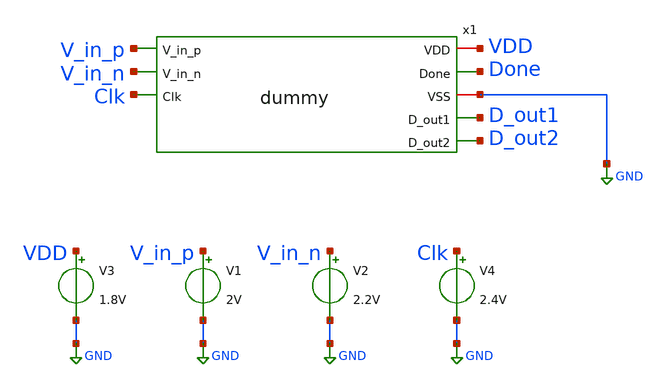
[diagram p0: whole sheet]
** sch_path: xschem/tests/dummy/dummy_test.sch
**.subckt dummy_test
V3 VDD GND 1.8V
x1 VDD V_in_p Done GND V_in_n D_out1 D_out2 Clk dummy
V1 V_in_p GND 2V
V2 V_in_n GND 2.2V
V4 Clk GND 2.4V
**** begin user architecture code
 .lib $::SKYWATER_MODELS/sky130.lib.spice tt
.include $::SKYWATER_STDCELLS/sky130_fd_sc_hd.spice


.options acct list savecurrents
.temp 25
*.probe I(x1)
.control
tran 0.1u 1u
* plot a b+2 clk+4 reset_b+6 x+8 y+10 q+12 qlatch+14
plot V_in_p D_out1
plot V_in_n D_out2
plot Clk Done
write dummy_test.raw
.endc


**** end user architecture code
**.ends
.GLOBAL GND
.end
